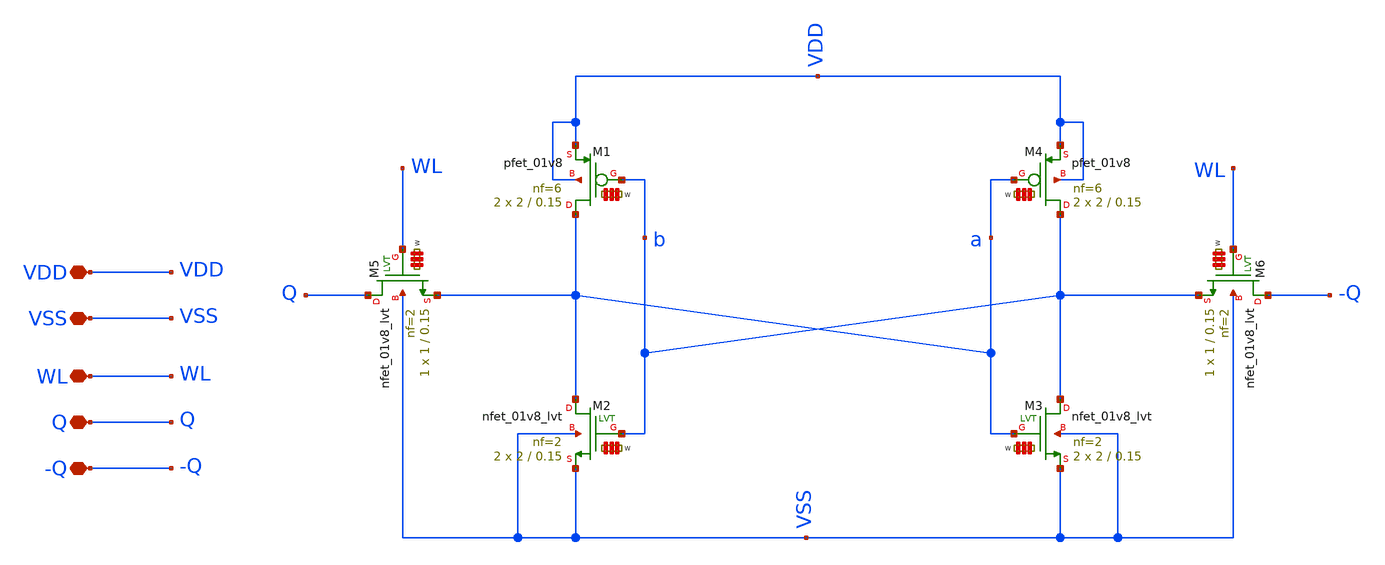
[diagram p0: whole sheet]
** sch_path: my_ip/LIB/Memory/SRAM_001_1_8_sky130A.sch
**.subckt SRAM_001_1_8_sky130A VDD VSS WL Q -Q
*.iopin VDD
*.iopin VSS
*.iopin WL
*.iopin Q
*.iopin -Q
XM1 a b VDD VDD sky130_fd_pr__pfet_01v8 L=0.15 W='2 * 6 ' nf=6 ad= as='int((6 + 2)/2) * 2 * 0.29' pd='2*int((6 + 1)/2) * (2 + 0.29)'
+ ps='2*int((6 + 2)/2) * (2 + 0.29)' nrd='0.29 / 2 / 6 ' nrs='0.29 / 2 / 6 ' sa=0 sb=0 sd=0 mult=2 m=2
XM2 a b VSS VSS sky130_fd_pr__nfet_01v8_lvt L=0.15 W='2 * 2 ' nf=2 ad='int((2 + 1)/2) * 2 / 2 * 0.29'
+ as='int((2 + 2)/2) * 2 / 2 * 0.29' pd='2*int((2 + 1)/2) * (2 / 2 + 0.29)' ps='2*int((2 + 2)/2) * (2 / 2 + 0.29)'
+ nrd='0.29 / 2 ' nrs='0.29 / 2 ' sa=0 sb=0 sd=0 mult=2 m=2
XM3 b a VSS VSS sky130_fd_pr__nfet_01v8_lvt L=0.15 W='2 * 2 ' nf=2 ad='int((2 + 1)/2) * 2 / 2 * 0.29'
+ as='int((2 + 2)/2) * 2 / 2 * 0.29' pd='2*int((2 + 1)/2) * (2 / 2 + 0.29)' ps='2*int((2 + 2)/2) * (2 / 2 + 0.29)'
+ nrd='0.29 / 2 ' nrs='0.29 / 2 ' sa=0 sb=0 sd=0 mult=2 m=2
XM4 b a VDD VDD sky130_fd_pr__pfet_01v8 L=0.15 W='2 * 6 ' nf=6 ad= as='int((6 + 2)/2) * 2 * 0.29' pd='2*int((6 + 1)/2) * (2 + 0.29)'
+ ps='2*int((6 + 2)/2) * (2 + 0.29)' nrd='0.29 / 2 / 6 ' nrs='0.29 / 2 / 6 ' sa=0 sb=0 sd=0 mult=2 m=2
XM5 Q WL a VSS sky130_fd_pr__nfet_01v8_lvt L=0.15 W='1 * 2 ' nf=2 ad='int((2 + 1)/2) * 1 / 2 * 0.29'
+ as='int((2 + 2)/2) * 1 / 2 * 0.29' pd='2*int((2 + 1)/2) * (1 / 2 + 0.29)' ps='2*int((2 + 2)/2) * (1 / 2 + 0.29)'
+ nrd='0.29 / 1 ' nrs='0.29 / 1 ' sa=0 sb=0 sd=0 mult=1 m=1
XM6 -Q WL b VSS sky130_fd_pr__nfet_01v8_lvt L=0.15 W='1 * 2 ' nf=2 ad='int((2 + 1)/2) * 1 / 2 * 0.29'
+ as='int((2 + 2)/2) * 1 / 2 * 0.29' pd='2*int((2 + 1)/2) * (1 / 2 + 0.29)' ps='2*int((2 + 2)/2) * (1 / 2 + 0.29)'
+ nrd='0.29 / 1 ' nrs='0.29 / 1 ' sa=0 sb=0 sd=0 mult=1 m=1
**.ends
.end
